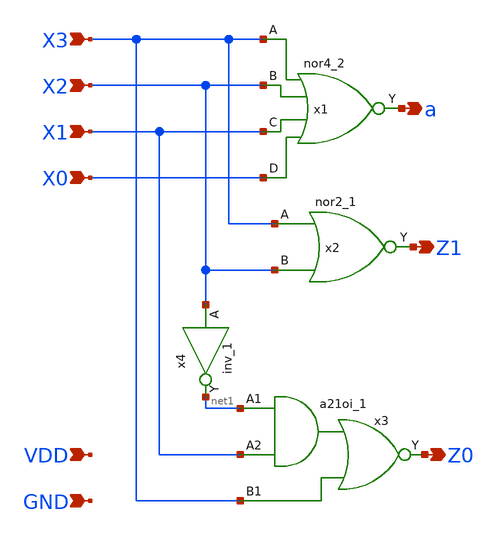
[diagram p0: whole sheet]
** sch_path: xschem/NLC_4bit.sch
**.subckt NLC_4bit X3 X2 X1 X0 a Z1 Z0 VDD GND
*.ipin X3
*.ipin X2
*.ipin X1
*.ipin X0
*.opin a
*.opin Z1
*.opin Z0
*.ipin VDD
*.ipin GND
x1 X3 X2 X1 X0 GND GND VDD VDD a sky130_fd_sc_hd__nor4_2
x2 X3 X2 GND GND VDD VDD Z1 sky130_fd_sc_hd__nor2_1
x3 net1 X1 X3 GND GND VDD VDD Z0 sky130_fd_sc_hd__a21oi_1
x4 X2 GND GND VDD VDD net1 sky130_fd_sc_hd__inv_1
**.ends
.end
